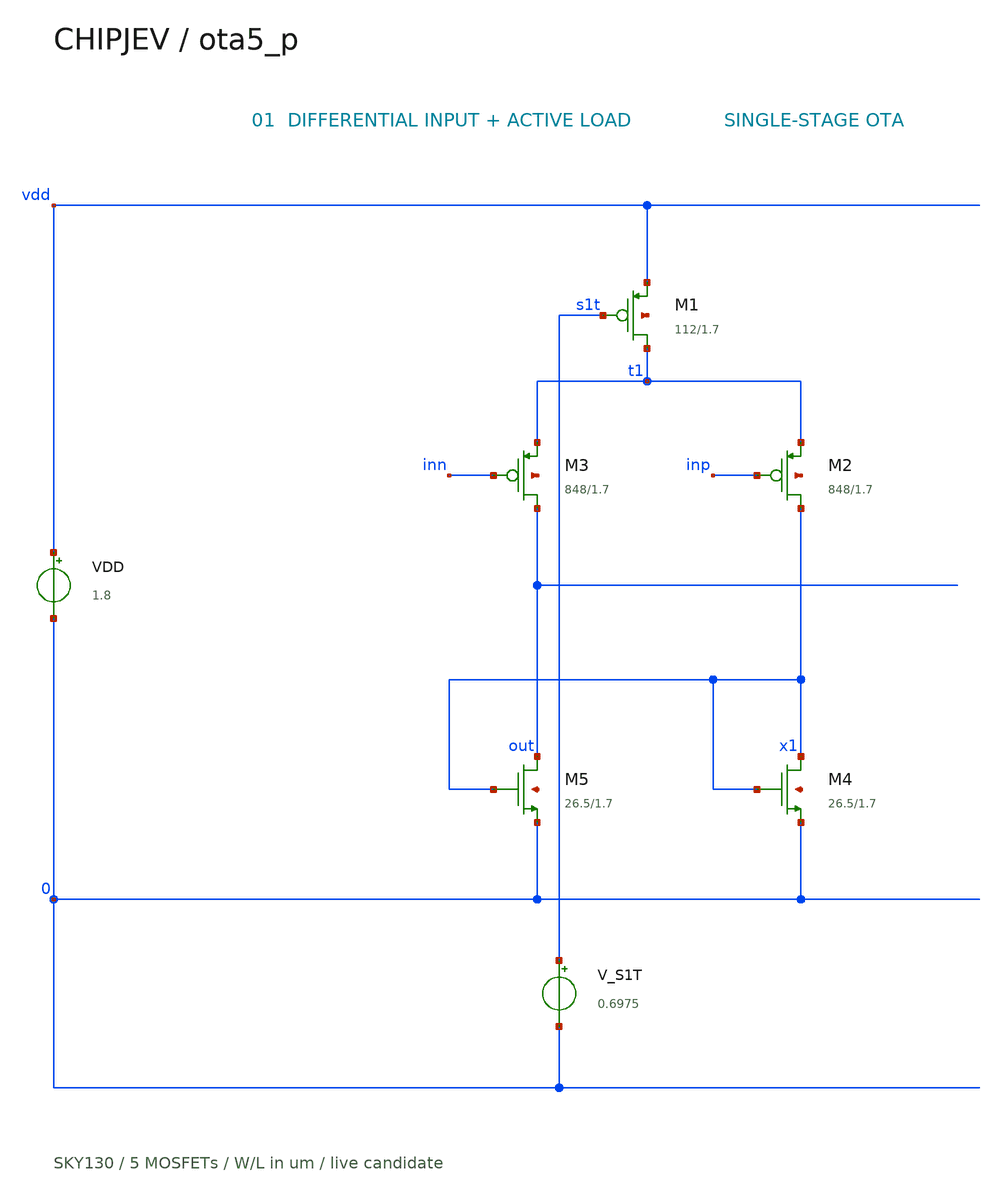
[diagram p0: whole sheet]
** sch_path: experiments/layout/results/ota-efficient/circuit.sch
**.subckt circuit
VDD vdd 0 1.8
XM1 t1 s1t vdd vdd sky130_fd_pr__pfet_01v8 L=1.69667 W=112.15 nf=3 ad=21.6823 as=21.6823 pd=150.693
+ ps=150.693 nrd=0.00258583 nrs=0.00258583 sa=0 sb=0 sd=0 mult=1 m=1
XM2 x1 inp t1 vdd sky130_fd_pr__pfet_01v8 L=1.69667 W=848.333 nf=17 ad=130.244 as=130.244 pd=903.455
+ ps=903.455 nrd=0.000341847 nrs=0.000341847 sa=0 sb=0 sd=0 mult=1 m=1
XM3 out inn t1 vdd sky130_fd_pr__pfet_01v8 L=1.69667 W=848.333 nf=17 ad=130.244 as=130.244
+ pd=903.455 ps=903.455 nrd=0.000341847 nrs=0.000341847 sa=0 sb=0 sd=0 mult=1 m=1
XM4 x1 x1 0 0 sky130_fd_pr__nfet_01v8 L=1.69667 W=26.468 nf=1 ad=7.67572 as=7.67572 pd=53.516
+ ps=53.516 nrd=0.0109566 nrs=0.0109566 sa=0 sb=0 sd=0 mult=1 m=1
XM5 out x1 0 0 sky130_fd_pr__nfet_01v8 L=1.69667 W=26.468 nf=1 ad=7.67572 as=7.67572 pd=53.516
+ ps=53.516 nrd=0.0109566 nrs=0.0109566 sa=0 sb=0 sd=0 mult=1 m=1
V_S1T s1t 0 0.6975
**.ends
.end
